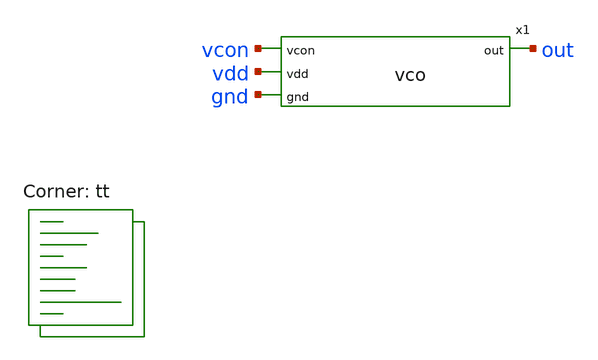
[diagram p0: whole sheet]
** sch_path: xschem/vco-tb.sch
**.subckt vco-tb
x1 vcon out vdd gnd vco
**** begin user architecture code
 .lib $::SKYWATER_MODELS/sky130.lib.spice tt

.param mc_mm_switch = 0
.param mc_pr_switch = 0




  .param val=0.5

  .option wnflag=1
  .option safecurrents

  Vvdd vdd gnd dc 1.8
  Vin vcon gnd dc {val}

  .control
    reset
    save all
    write vco-tb.raw
    set appendwrite

    let vval=0
    while vval <= 1.8
      alterparam val=$&vval
      reset
      save all
      tran 0.01n 500n
      write vco-tb.raw
      let vval = vval + 0.1
    end
    quit 0
  .endc



**** end user architecture code
**.ends

* expanding   symbol:  vco.sym # of pins=4
** sym_path: xschem/vco.sym
** sch_path: xschem/vco.sch
.subckt vco vcon out vdd gnd
*.ipin vcon
*.opin out
*.ipin vdd
*.ipin gnd
.param wpo=4.8 lpo=0.54 wno=2.4 lno=0.54 wpcb=4.8 lpcb=0.36 wncb=0.96 lncb=0.36 wpvb=6 lpvb=0.9
+ wnvc=96 lnvc=0.9 wpbuff=4.8 lpbuff=0.18 wnbuff=1.2 lnbuff=0.18 lres=3.5

XM1 vnbias vnbias gnd gnd sky130_fd_pr__nfet_01v8 L=lncb W=wncb nf=1 ad='int((nf+1)/2) * W/nf * 0.29'
+ as='int((nf+2)/2) * W/nf * 0.29' pd='2*int((nf+1)/2) * (W/nf + 0.29)' ps='2*int((nf+2)/2) * (W/nf + 0.29)'
+ nrd='0.29 / W' nrs='0.29 / W' sa=0 sb=0 sd=0 mult=1 m=1
XM2 vpbias vpbias vdd vdd sky130_fd_pr__pfet_01v8 L=lpvb W=wpvb nf=1 ad='int((nf+1)/2) * W/nf * 0.29'
+ as='int((nf+2)/2) * W/nf * 0.29' pd='2*int((nf+1)/2) * (W/nf + 0.29)' ps='2*int((nf+2)/2) * (W/nf + 0.29)'
+ nrd='0.29 / W' nrs='0.29 / W' sa=0 sb=0 sd=0 mult=1 m=1
XM4 vnbias vpbias vdd vdd sky130_fd_pr__pfet_01v8 L=lpcb W=wpcb nf=1 ad='int((nf+1)/2) * W/nf * 0.29'
+ as='int((nf+2)/2) * W/nf * 0.29' pd='2*int((nf+1)/2) * (W/nf + 0.29)' ps='2*int((nf+2)/2) * (W/nf + 0.29)'
+ nrd='0.29 / W' nrs='0.29 / W' sa=0 sb=0 sd=0 mult=1 m=1
XM5 net8 net9 net1 gnd sky130_fd_pr__nfet_01v8 L=lno W=wno nf=1 ad='int((nf+1)/2) * W/nf * 0.29' as='int((nf+2)/2) * W/nf * 0.29'
+ pd='2*int((nf+1)/2) * (W/nf + 0.29)' ps='2*int((nf+2)/2) * (W/nf + 0.29)' nrd='0.29 / W' nrs='0.29 / W'
+ sa=0 sb=0 sd=0 mult=1 m=1
XM6 net8 net9 net12 vdd sky130_fd_pr__pfet_01v8 L=lpo W=wpo nf=1 ad='int((nf+1)/2) * W/nf * 0.29' as='int((nf+2)/2) * W/nf * 0.29'
+ pd='2*int((nf+1)/2) * (W/nf + 0.29)' ps='2*int((nf+2)/2) * (W/nf + 0.29)' nrd='0.29 / W' nrs='0.29 / W'
+ sa=0 sb=0 sd=0 mult=1 m=1
XM7 net7 net8 net2 gnd sky130_fd_pr__nfet_01v8 L=lno W=wno nf=1 ad='int((nf+1)/2) * W/nf * 0.29' as='int((nf+2)/2) * W/nf * 0.29'
+ pd='2*int((nf+1)/2) * (W/nf + 0.29)' ps='2*int((nf+2)/2) * (W/nf + 0.29)' nrd='0.29 / W' nrs='0.29 / W'
+ sa=0 sb=0 sd=0 mult=1 m=1
XM8 net7 net8 net13 vdd sky130_fd_pr__pfet_01v8 L=lpo W=wpo nf=1 ad='int((nf+1)/2) * W/nf * 0.29' as='int((nf+2)/2) * W/nf * 0.29'
+ pd='2*int((nf+1)/2) * (W/nf + 0.29)' ps='2*int((nf+2)/2) * (W/nf + 0.29)' nrd='0.29 / W' nrs='0.29 / W'
+ sa=0 sb=0 sd=0 mult=1 m=1
XM9 net6 net7 net3 gnd sky130_fd_pr__nfet_01v8 L=lno W=wno nf=1 ad='int((nf+1)/2) * W/nf * 0.29' as='int((nf+2)/2) * W/nf * 0.29'
+ pd='2*int((nf+1)/2) * (W/nf + 0.29)' ps='2*int((nf+2)/2) * (W/nf + 0.29)' nrd='0.29 / W' nrs='0.29 / W'
+ sa=0 sb=0 sd=0 mult=1 m=1
XM10 net6 net7 net14 vdd sky130_fd_pr__pfet_01v8 L=lpo W=wpo nf=1 ad='int((nf+1)/2) * W/nf * 0.29' as='int((nf+2)/2) * W/nf * 0.29'
+ pd='2*int((nf+1)/2) * (W/nf + 0.29)' ps='2*int((nf+2)/2) * (W/nf + 0.29)' nrd='0.29 / W' nrs='0.29 / W'
+ sa=0 sb=0 sd=0 mult=1 m=1
XM11 net10 net6 net5 gnd sky130_fd_pr__nfet_01v8 L=lno W=wno nf=1 ad='int((nf+1)/2) * W/nf * 0.29' as='int((nf+2)/2) * W/nf * 0.29'
+ pd='2*int((nf+1)/2) * (W/nf + 0.29)' ps='2*int((nf+2)/2) * (W/nf + 0.29)' nrd='0.29 / W' nrs='0.29 / W'
+ sa=0 sb=0 sd=0 mult=1 m=1
XM12 net10 net6 net15 vdd sky130_fd_pr__pfet_01v8 L=lpo W=wpo nf=1 ad='int((nf+1)/2) * W/nf * 0.29' as='int((nf+2)/2) * W/nf * 0.29'
+ pd='2*int((nf+1)/2) * (W/nf + 0.29)' ps='2*int((nf+2)/2) * (W/nf + 0.29)' nrd='0.29 / W' nrs='0.29 / W'
+ sa=0 sb=0 sd=0 mult=1 m=1
XM13 net9 net10 net4 gnd sky130_fd_pr__nfet_01v8 L=lno W=wno nf=1 ad='int((nf+1)/2) * W/nf * 0.29' as='int((nf+2)/2) * W/nf * 0.29'
+ pd='2*int((nf+1)/2) * (W/nf + 0.29)' ps='2*int((nf+2)/2) * (W/nf + 0.29)' nrd='0.29 / W' nrs='0.29 / W'
+ sa=0 sb=0 sd=0 mult=1 m=1
XM14 net9 net10 net16 vdd sky130_fd_pr__pfet_01v8 L=lpo W=wpo nf=1 ad='int((nf+1)/2) * W/nf * 0.29' as='int((nf+2)/2) * W/nf * 0.29'
+ pd='2*int((nf+1)/2) * (W/nf + 0.29)' ps='2*int((nf+2)/2) * (W/nf + 0.29)' nrd='0.29 / W' nrs='0.29 / W'
+ sa=0 sb=0 sd=0 mult=1 m=1
XM16 net12 vpbias vdd vdd sky130_fd_pr__pfet_01v8 L=lpcb W=wpcb nf=1 ad='int((nf+1)/2) * W/nf * 0.29'
+ as='int((nf+2)/2) * W/nf * 0.29' pd='2*int((nf+1)/2) * (W/nf + 0.29)' ps='2*int((nf+2)/2) * (W/nf + 0.29)'
+ nrd='0.29 / W' nrs='0.29 / W' sa=0 sb=0 sd=0 mult=1 m=1
XM18 net13 vpbias vdd vdd sky130_fd_pr__pfet_01v8 L=lpcb W=wpcb nf=1 ad='int((nf+1)/2) * W/nf * 0.29'
+ as='int((nf+2)/2) * W/nf * 0.29' pd='2*int((nf+1)/2) * (W/nf + 0.29)' ps='2*int((nf+2)/2) * (W/nf + 0.29)'
+ nrd='0.29 / W' nrs='0.29 / W' sa=0 sb=0 sd=0 mult=1 m=1
XM20 net14 vpbias vdd vdd sky130_fd_pr__pfet_01v8 L=lpcb W=wpcb nf=1 ad='int((nf+1)/2) * W/nf * 0.29'
+ as='int((nf+2)/2) * W/nf * 0.29' pd='2*int((nf+1)/2) * (W/nf + 0.29)' ps='2*int((nf+2)/2) * (W/nf + 0.29)'
+ nrd='0.29 / W' nrs='0.29 / W' sa=0 sb=0 sd=0 mult=1 m=1
XM22 net15 vpbias vdd vdd sky130_fd_pr__pfet_01v8 L=lpcb W=wpcb nf=1 ad='int((nf+1)/2) * W/nf * 0.29'
+ as='int((nf+2)/2) * W/nf * 0.29' pd='2*int((nf+1)/2) * (W/nf + 0.29)' ps='2*int((nf+2)/2) * (W/nf + 0.29)'
+ nrd='0.29 / W' nrs='0.29 / W' sa=0 sb=0 sd=0 mult=1 m=1
XM24 net16 vpbias vdd vdd sky130_fd_pr__pfet_01v8 L=lpcb W=wpcb nf=1 ad='int((nf+1)/2) * W/nf * 0.29'
+ as='int((nf+2)/2) * W/nf * 0.29' pd='2*int((nf+1)/2) * (W/nf + 0.29)' ps='2*int((nf+2)/2) * (W/nf + 0.29)'
+ nrd='0.29 / W' nrs='0.29 / W' sa=0 sb=0 sd=0 mult=1 m=1
XM25 net11 net9 gnd gnd sky130_fd_pr__nfet_01v8 L=lnbuff W=wnbuff nf=1 ad='int((nf+1)/2) * W/nf * 0.29'
+ as='int((nf+2)/2) * W/nf * 0.29' pd='2*int((nf+1)/2) * (W/nf + 0.29)' ps='2*int((nf+2)/2) * (W/nf + 0.29)'
+ nrd='0.29 / W' nrs='0.29 / W' sa=0 sb=0 sd=0 mult=1 m=1
XM26 net11 net9 vdd vdd sky130_fd_pr__pfet_01v8 L=lpbuff W=wpbuff nf=1 ad='int((nf+1)/2) * W/nf * 0.29'
+ as='int((nf+2)/2) * W/nf * 0.29' pd='2*int((nf+1)/2) * (W/nf + 0.29)' ps='2*int((nf+2)/2) * (W/nf + 0.29)'
+ nrd='0.29 / W' nrs='0.29 / W' sa=0 sb=0 sd=0 mult=1 m=1
XM27 out net11 gnd gnd sky130_fd_pr__nfet_01v8 L=lnbuff W=wnbuff nf=1 ad='int((nf+1)/2) * W/nf * 0.29'
+ as='int((nf+2)/2) * W/nf * 0.29' pd='2*int((nf+1)/2) * (W/nf + 0.29)' ps='2*int((nf+2)/2) * (W/nf + 0.29)'
+ nrd='0.29 / W' nrs='0.29 / W' sa=0 sb=0 sd=0 mult=1 m=1
XM28 out net11 vdd vdd sky130_fd_pr__pfet_01v8 L=lpbuff W=wpbuff nf=1 ad='int((nf+1)/2) * W/nf * 0.29'
+ as='int((nf+2)/2) * W/nf * 0.29' pd='2*int((nf+1)/2) * (W/nf + 0.29)' ps='2*int((nf+2)/2) * (W/nf + 0.29)'
+ nrd='0.29 / W' nrs='0.29 / W' sa=0 sb=0 sd=0 mult=1 m=1
XM15 net1 vnbias gnd gnd sky130_fd_pr__nfet_01v8 L=lncb W=wncb nf=1 ad='int((nf+1)/2) * W/nf * 0.29'
+ as='int((nf+2)/2) * W/nf * 0.29' pd='2*int((nf+1)/2) * (W/nf + 0.29)' ps='2*int((nf+2)/2) * (W/nf + 0.29)'
+ nrd='0.29 / W' nrs='0.29 / W' sa=0 sb=0 sd=0 mult=1 m=1
XM17 net2 vnbias gnd gnd sky130_fd_pr__nfet_01v8 L=lncb W=wncb nf=1 ad='int((nf+1)/2) * W/nf * 0.29'
+ as='int((nf+2)/2) * W/nf * 0.29' pd='2*int((nf+1)/2) * (W/nf + 0.29)' ps='2*int((nf+2)/2) * (W/nf + 0.29)'
+ nrd='0.29 / W' nrs='0.29 / W' sa=0 sb=0 sd=0 mult=1 m=1
XM19 net3 vnbias gnd gnd sky130_fd_pr__nfet_01v8 L=lncb W=wncb nf=1 ad='int((nf+1)/2) * W/nf * 0.29'
+ as='int((nf+2)/2) * W/nf * 0.29' pd='2*int((nf+1)/2) * (W/nf + 0.29)' ps='2*int((nf+2)/2) * (W/nf + 0.29)'
+ nrd='0.29 / W' nrs='0.29 / W' sa=0 sb=0 sd=0 mult=1 m=1
XM21 net5 vnbias gnd gnd sky130_fd_pr__nfet_01v8 L=lncb W=wncb nf=1 ad='int((nf+1)/2) * W/nf * 0.29'
+ as='int((nf+2)/2) * W/nf * 0.29' pd='2*int((nf+1)/2) * (W/nf + 0.29)' ps='2*int((nf+2)/2) * (W/nf + 0.29)'
+ nrd='0.29 / W' nrs='0.29 / W' sa=0 sb=0 sd=0 mult=1 m=1
XM23 net4 vnbias gnd gnd sky130_fd_pr__nfet_01v8 L=lncb W=wncb nf=1 ad='int((nf+1)/2) * W/nf * 0.29'
+ as='int((nf+2)/2) * W/nf * 0.29' pd='2*int((nf+1)/2) * (W/nf + 0.29)' ps='2*int((nf+2)/2) * (W/nf + 0.29)'
+ nrd='0.29 / W' nrs='0.29 / W' sa=0 sb=0 sd=0 mult=1 m=1
XR3 gnd net17 gnd sky130_fd_pr__res_xhigh_po W=0.35 L=lres mult=1 m=1
XM29 vpbias vcon net17 gnd sky130_fd_pr__nfet_01v8 L=lnvc W=wnvc nf=1 ad='int((nf+1)/2) * W/nf * 0.29'
+ as='int((nf+2)/2) * W/nf * 0.29' pd='2*int((nf+1)/2) * (W/nf + 0.29)' ps='2*int((nf+2)/2) * (W/nf + 0.29)'
+ nrd='0.29 / W' nrs='0.29 / W' sa=0 sb=0 sd=0 mult=1 m=1
.ends

.end
